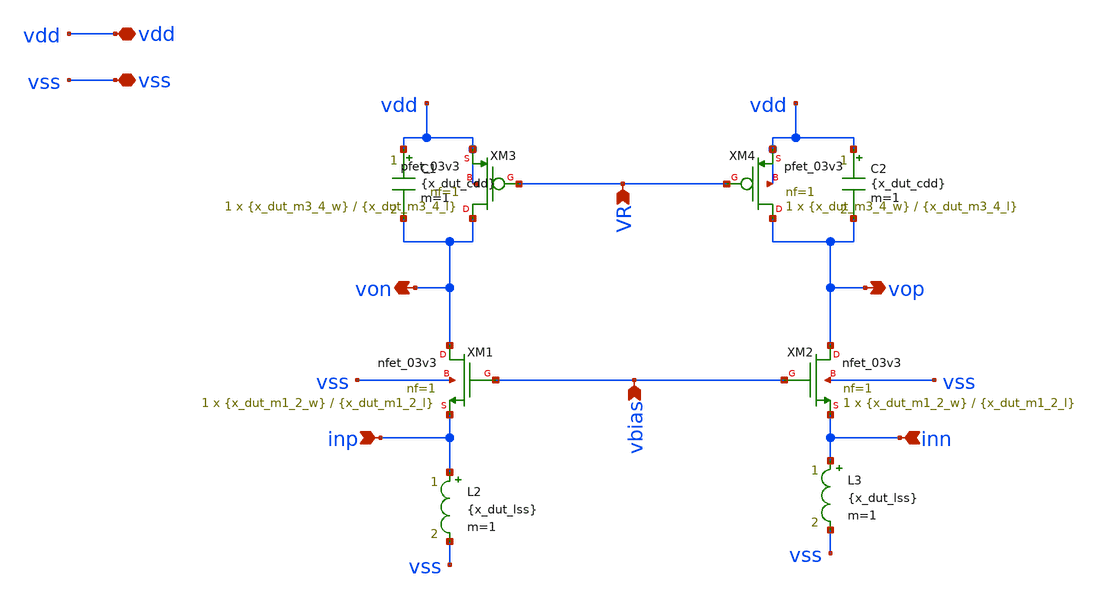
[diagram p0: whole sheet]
** sch_path: examples/tunable-tia/gf180/tia-bpf-2/bpf-tia-2.sch
**.subckt bpf-tia-2 vdd vss inp inn von vop vbias VR
*.iopin vdd
*.iopin vss
*.ipin inp
*.ipin inn
*.opin von
*.opin vop
*.ipin vbias
*.ipin VR
XM1 von vbias inp vss nfet_03v3 L={x_dut_m1_2_l} W={x_dut_m1_2_w} nf=1 ad='int((nf+1)/2) * W/nf * 0.18u'
+ as='int((nf+2)/2) * W/nf * 0.18u' pd='2*int((nf+1)/2) * (W/nf + 0.18u)' ps='2*int((nf+2)/2) * (W/nf + 0.18u)'
+ nrd='0.18u / W' nrs='0.18u / W' sa=0 sb=0 sd=0 m=1
XM2 vop vbias inn vss nfet_03v3 L={x_dut_m1_2_l} W={x_dut_m1_2_w} nf=1 ad='int((nf+1)/2) * W/nf * 0.18u'
+ as='int((nf+2)/2) * W/nf * 0.18u' pd='2*int((nf+1)/2) * (W/nf + 0.18u)' ps='2*int((nf+2)/2) * (W/nf + 0.18u)'
+ nrd='0.18u / W' nrs='0.18u / W' sa=0 sb=0 sd=0 m=1
C1 vdd von {x_dut_cdd} m=1
C2 vdd vop {x_dut_cdd} m=1
XM3 von VR vdd vdd pfet_03v3 L={x_dut_m3_4_l} W={x_dut_m3_4_w} nf=1 ad='int((nf+1)/2) * W/nf * 0.18u'
+ as='int((nf+2)/2) * W/nf * 0.18u' pd='2*int((nf+1)/2) * (W/nf + 0.18u)' ps='2*int((nf+2)/2) * (W/nf + 0.18u)'
+ nrd='0.18u / W' nrs='0.18u / W' sa=0 sb=0 sd=0 m=1
XM4 vop VR vdd vdd pfet_03v3 L={x_dut_m3_4_l} W={x_dut_m3_4_w} nf=1 ad='int((nf+1)/2) * W/nf * 0.18u'
+ as='int((nf+2)/2) * W/nf * 0.18u' pd='2*int((nf+1)/2) * (W/nf + 0.18u)' ps='2*int((nf+2)/2) * (W/nf + 0.18u)'
+ nrd='0.18u / W' nrs='0.18u / W' sa=0 sb=0 sd=0 m=1
L2 inp vss {x_dut_lss} m=1
L3 inn vss {x_dut_lss} m=1
**.ends
.end
